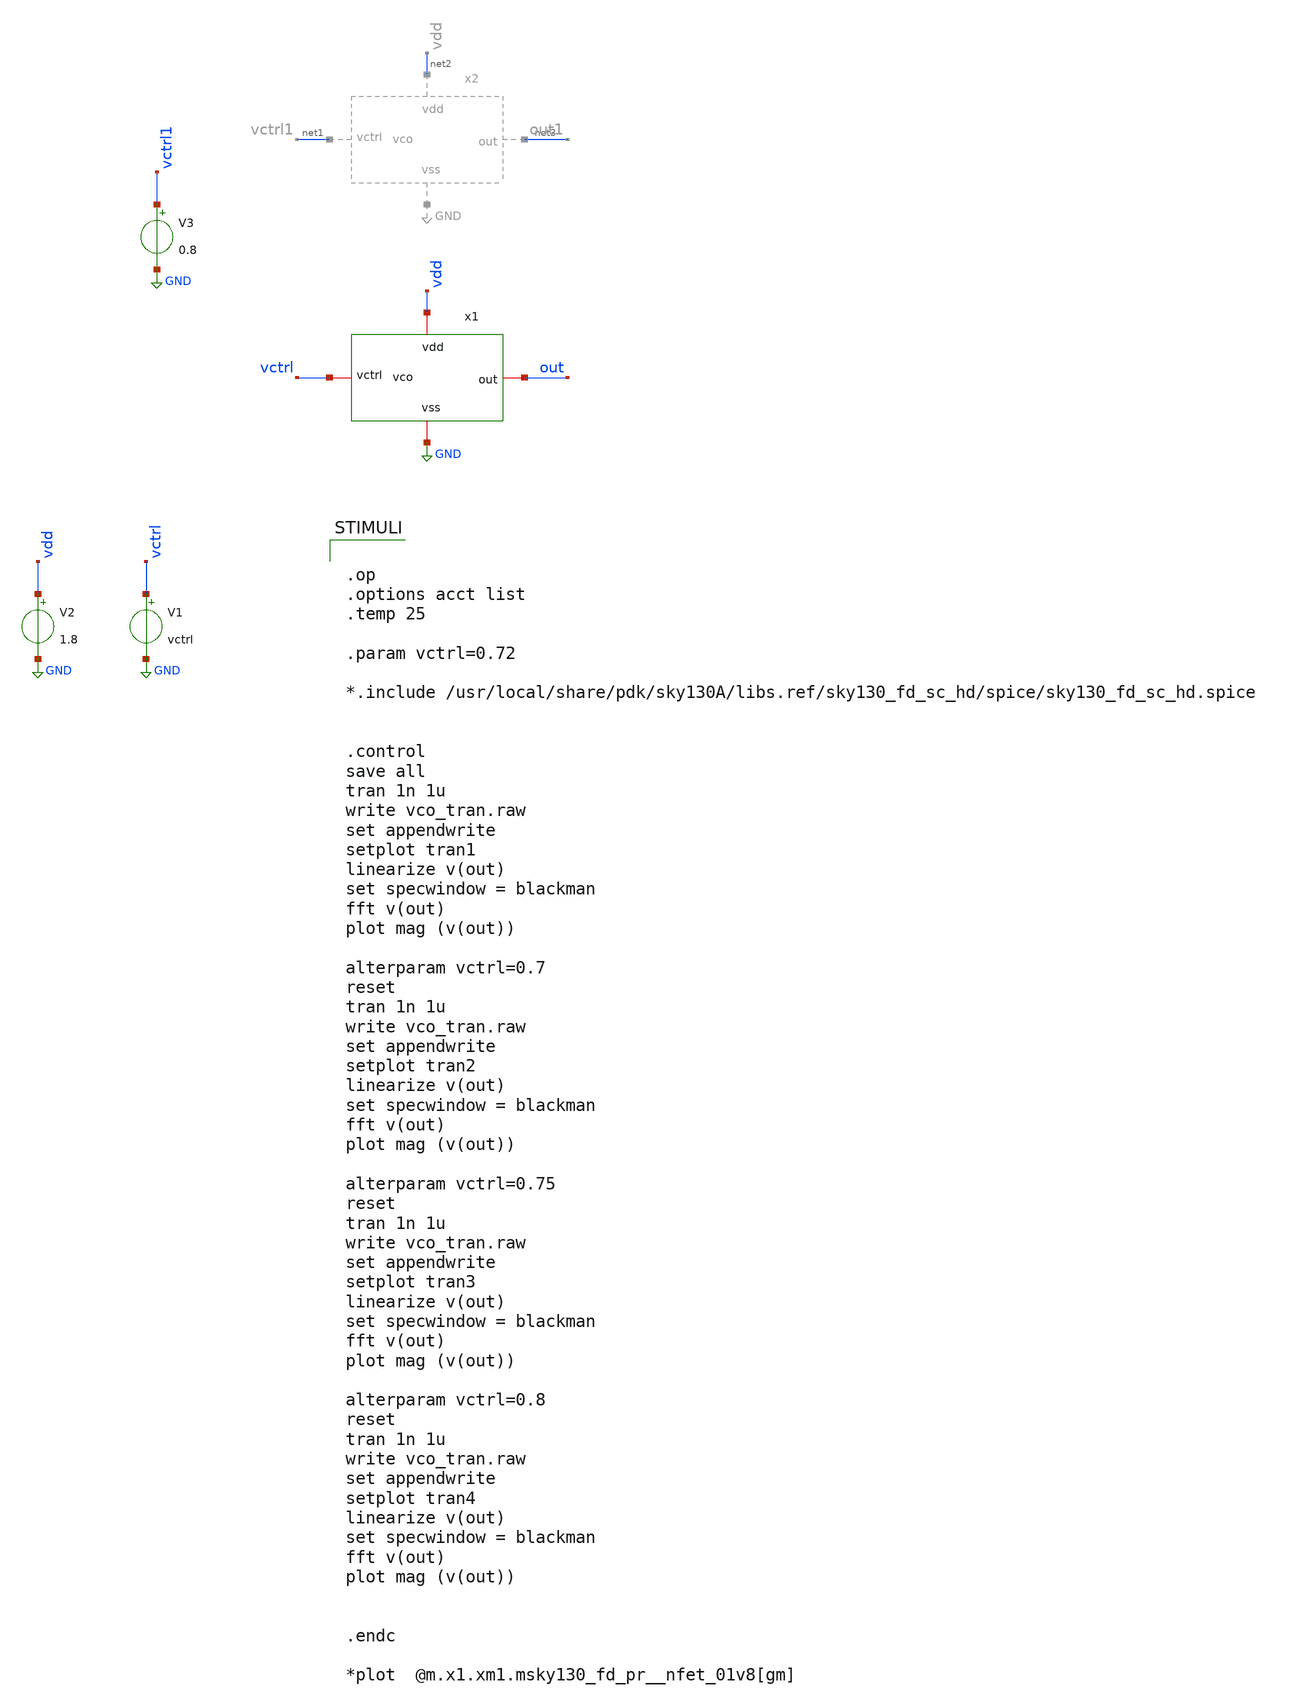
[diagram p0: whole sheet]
** sch_path: xschem01/vco/vco_tran.sch
**.subckt vco_tran
x1 vdd out vctrl GND vco
V1 vctrl GND vctrl
V2 vdd GND 1.8
V3 vctrl1 GND 0.8
**** begin user architecture code


.op
.options acct list
.temp 25

.param vctrl=0.72

*.include /usr/local/share/pdk/sky130A/libs.ref/sky130_fd_sc_hd/spice/sky130_fd_sc_hd.spice


.control
save all
tran 1n 1u
write vco_tran.raw
set appendwrite
setplot tran1
linearize v(out)
set specwindow = blackman
fft v(out)
plot mag (v(out))

alterparam vctrl=0.7
reset
tran 1n 1u
write vco_tran.raw
set appendwrite
setplot tran2
linearize v(out)
set specwindow = blackman
fft v(out)
plot mag (v(out))

alterparam vctrl=0.75
reset
tran 1n 1u
write vco_tran.raw
set appendwrite
setplot tran3
linearize v(out)
set specwindow = blackman
fft v(out)
plot mag (v(out))

alterparam vctrl=0.8
reset
tran 1n 1u
write vco_tran.raw
set appendwrite
setplot tran4
linearize v(out)
set specwindow = blackman
fft v(out)
plot mag (v(out))


.endc

*plot  @m.x1.xm1.msky130_fd_pr__nfet_01v8[gm]



** opencircuitdesign pdks install
.lib $::SKYWATER_MODELS/sky130.lib.spice tt


**** end user architecture code
**.ends

* expanding   symbol:  vco/vco.sym # of pins=4
** sym_path: xschem01/vco/vco.sym
** sch_path: xschem01/vco/vco.sch
.subckt vco vdd out vctrl vss
*.iopin vdd
*.iopin vss
*.iopin out
*.iopin vctrl
XM1 net1 vctrl vss vss sky130_fd_pr__nfet_01v8 L=0.15 W=30 nf=1 ad='int((nf+1)/2) * W/nf * 0.29' as='int((nf+2)/2) * W/nf * 0.29'
+ pd='2*int((nf+1)/2) * (W/nf + 0.29)' ps='2*int((nf+2)/2) * (W/nf + 0.29)' nrd='0.29 / W' nrs='0.29 / W'
+ sa=0 sb=0 sd=0 mult=1 m=1
XM2 net1 net1 vdd vdd sky130_fd_pr__pfet_01v8 L=0.15 W=90 nf=1 ad='int((nf+1)/2) * W/nf * 0.29' as='int((nf+2)/2) * W/nf * 0.29'
+ pd='2*int((nf+1)/2) * (W/nf + 0.29)' ps='2*int((nf+2)/2) * (W/nf + 0.29)' nrd='0.29 / W' nrs='0.29 / W'
+ sa=0 sb=0 sd=0 mult=1 m=1
XM3 net4 net1 vdd vdd sky130_fd_pr__pfet_01v8 L=0.15 W=80 nf=1 ad='int((nf+1)/2) * W/nf * 0.29' as='int((nf+2)/2) * W/nf * 0.29'
+ pd='2*int((nf+1)/2) * (W/nf + 0.29)' ps='2*int((nf+2)/2) * (W/nf + 0.29)' nrd='0.29 / W' nrs='0.29 / W'
+ sa=0 sb=0 sd=0 mult=1 m=1
XM4 net3 out net4 net4 sky130_fd_pr__pfet_01v8 L=0.15 W=80 nf=1 ad='int((nf+1)/2) * W/nf * 0.29' as='int((nf+2)/2) * W/nf * 0.29'
+ pd='2*int((nf+1)/2) * (W/nf + 0.29)' ps='2*int((nf+2)/2) * (W/nf + 0.29)' nrd='0.29 / W' nrs='0.29 / W'
+ sa=0 sb=0 sd=0 mult=1 m=1
XM5 net2 vctrl vss vss sky130_fd_pr__nfet_01v8 L=0.15 W=30 nf=1 ad='int((nf+1)/2) * W/nf * 0.29' as='int((nf+2)/2) * W/nf * 0.29'
+ pd='2*int((nf+1)/2) * (W/nf + 0.29)' ps='2*int((nf+2)/2) * (W/nf + 0.29)' nrd='0.29 / W' nrs='0.29 / W'
+ sa=0 sb=0 sd=0 mult=1 m=1
XM6 net3 out net2 vss sky130_fd_pr__nfet_01v8 L=0.15 W=30 nf=1 ad='int((nf+1)/2) * W/nf * 0.29' as='int((nf+2)/2) * W/nf * 0.29'
+ pd='2*int((nf+1)/2) * (W/nf + 0.29)' ps='2*int((nf+2)/2) * (W/nf + 0.29)' nrd='0.29 / W' nrs='0.29 / W'
+ sa=0 sb=0 sd=0 mult=1 m=1
XM7 net7 net1 vdd vdd sky130_fd_pr__pfet_01v8 L=0.15 W=80 nf=1 ad='int((nf+1)/2) * W/nf * 0.29' as='int((nf+2)/2) * W/nf * 0.29'
+ pd='2*int((nf+1)/2) * (W/nf + 0.29)' ps='2*int((nf+2)/2) * (W/nf + 0.29)' nrd='0.29 / W' nrs='0.29 / W'
+ sa=0 sb=0 sd=0 mult=2 m=2
XM8 net6 net3 net7 net7 sky130_fd_pr__pfet_01v8 L=0.15 W=80 nf=1 ad='int((nf+1)/2) * W/nf * 0.29' as='int((nf+2)/2) * W/nf * 0.29'
+ pd='2*int((nf+1)/2) * (W/nf + 0.29)' ps='2*int((nf+2)/2) * (W/nf + 0.29)' nrd='0.29 / W' nrs='0.29 / W'
+ sa=0 sb=0 sd=0 mult=2 m=2
XM9 net5 vctrl vss vss sky130_fd_pr__nfet_01v8 L=0.15 W=60 nf=1 ad='int((nf+1)/2) * W/nf * 0.29' as='int((nf+2)/2) * W/nf * 0.29'
+ pd='2*int((nf+1)/2) * (W/nf + 0.29)' ps='2*int((nf+2)/2) * (W/nf + 0.29)' nrd='0.29 / W' nrs='0.29 / W'
+ sa=0 sb=0 sd=0 mult=1 m=1
XM10 net6 net3 net5 vss sky130_fd_pr__nfet_01v8 L=0.15 W=60 nf=1 ad='int((nf+1)/2) * W/nf * 0.29' as='int((nf+2)/2) * W/nf * 0.29'
+ pd='2*int((nf+1)/2) * (W/nf + 0.29)' ps='2*int((nf+2)/2) * (W/nf + 0.29)' nrd='0.29 / W' nrs='0.29 / W'
+ sa=0 sb=0 sd=0 mult=1 m=1
XM11 net9 net1 vdd vdd sky130_fd_pr__pfet_01v8 L=0.15 W=80 nf=1 ad='int((nf+1)/2) * W/nf * 0.29' as='int((nf+2)/2) * W/nf * 0.29'
+ pd='2*int((nf+1)/2) * (W/nf + 0.29)' ps='2*int((nf+2)/2) * (W/nf + 0.29)' nrd='0.29 / W' nrs='0.29 / W'
+ sa=0 sb=0 sd=0 mult=3 m=3
XM12 out net6 net9 net9 sky130_fd_pr__pfet_01v8 L=0.15 W=80 nf=1 ad='int((nf+1)/2) * W/nf * 0.29' as='int((nf+2)/2) * W/nf * 0.29'
+ pd='2*int((nf+1)/2) * (W/nf + 0.29)' ps='2*int((nf+2)/2) * (W/nf + 0.29)' nrd='0.29 / W' nrs='0.29 / W'
+ sa=0 sb=0 sd=0 mult=3 m=3
XM13 net8 vctrl vss vss sky130_fd_pr__nfet_01v8 L=0.15 W=90 nf=1 ad='int((nf+1)/2) * W/nf * 0.29' as='int((nf+2)/2) * W/nf * 0.29'
+ pd='2*int((nf+1)/2) * (W/nf + 0.29)' ps='2*int((nf+2)/2) * (W/nf + 0.29)' nrd='0.29 / W' nrs='0.29 / W'
+ sa=0 sb=0 sd=0 mult=1 m=1
XM14 out net6 net8 vss sky130_fd_pr__nfet_01v8 L=0.15 W=90 nf=1 ad='int((nf+1)/2) * W/nf * 0.29' as='int((nf+2)/2) * W/nf * 0.29'
+ pd='2*int((nf+1)/2) * (W/nf + 0.29)' ps='2*int((nf+2)/2) * (W/nf + 0.29)' nrd='0.29 / W' nrs='0.29 / W'
+ sa=0 sb=0 sd=0 mult=1 m=1
.ends

.GLOBAL GND
.end
